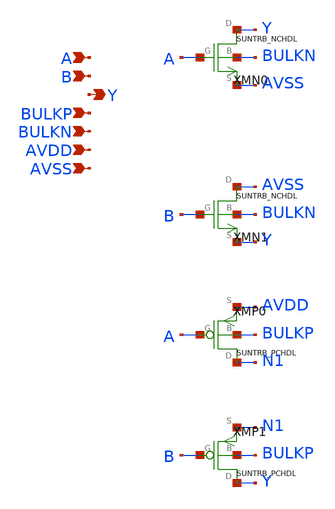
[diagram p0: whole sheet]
** sch_path: ip/sun_trb_sky130nm/design/SUN_TRB_SKY130NM/SUNTRB_NRX1_CV.sch
**.subckt SUNTRB_NRX1_CV A B Y BULKP BULKN AVDD AVSS
*.ipin A
*.ipin B
*.opin Y
*.ipin BULKP
*.ipin BULKN
*.ipin AVDD
*.ipin AVSS
XMN0 Y A AVSS BULKN SUNTRB_NCHDL xoffset=0 yoffset=0 angle=0
XMN1 AVSS B Y BULKN SUNTRB_NCHDL xoffset=0 yoffset=0 angle=0
XMP0 N1 A AVDD BULKP SUNTRB_PCHDL xoffset=0 yoffset=0 angle=0
XMP1 Y B N1 BULKP SUNTRB_PCHDL xoffset=0 yoffset=0 angle=0
**.ends
.end
